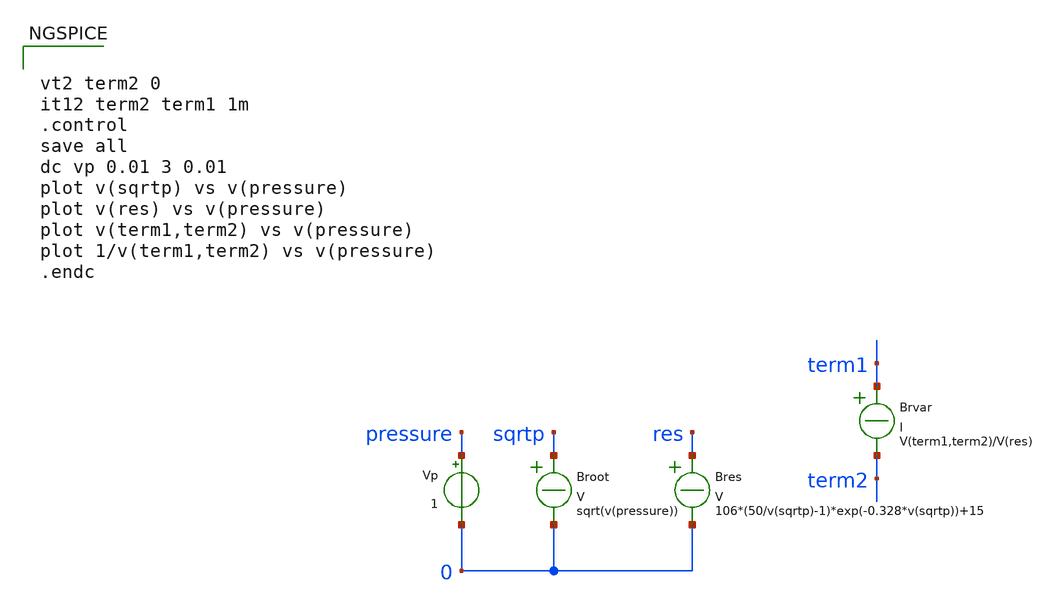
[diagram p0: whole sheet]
** sch_path: sensormodels/b_source_magic.sch
* Copyright 2020 Stefan Frederik Schippers
* Licensed under the Apache License, Version 2.0 (the "License");
* you may not use this file except in compliance with the License.
* You may obtain a copy of the License at
* https://www.apache.org/licenses/LICENSE-2.0
* Unless required by applicable law or agreed to in writing, software
* distributed under the License is distributed on an "AS IS" BASIS,
* WITHOUT WARRANTIES OR CONDITIONS OF ANY KIND, either express or implied.
* See the License for the specific language governing permissions and
* limitations under the License.
**.subckt b_source_magic
Broot sqrtp 0 V = sqrt(v(pressure))
Vp pressure 0 1
Bres res 0 V = 106*(50/v(sqrtp)-1)*exp(-0.328*v(sqrtp))+15
Brvar term1 term2 I = V(term1,term2)/V(res)
**** begin user architecture code


vt2 term2 0
it12 term2 term1 1m
.control
save all
dc vp 0.01 3 0.01
plot v(sqrtp) vs v(pressure)
plot v(res) vs v(pressure)
plot v(term1,term2) vs v(pressure)
plot 1/v(term1,term2) vs v(pressure)
.endc


 .lib $::SKYWATER_MODELS/models/sky130.lib.spice tt

.param mc_mm_switch=0
.param mc_pr_switch=1


**** end user architecture code
**.ends
.end
